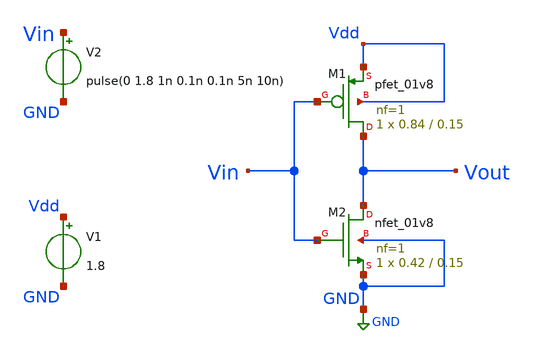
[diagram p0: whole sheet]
** sch_path: xschem_project/inverter/inverter_tb.sch
**.subckt inverter_tb
XM1 Vout Vin Vdd Vdd sky130_fd_pr__pfet_01v8 L=0.15 W=0.84 nf=1 ad='int((1 + 1)/2) * 0.84 / 1 * 0.29'
+ as='int((1 + 2)/2) * 0.84 / 1 * 0.29' pd='2*int((1 + 1)/2) * (0.84 / 1 + 0.29)' ps='2*int((1 + 2)/2) * (0.84 / 1 + 0.29)'
+ nrd='0.29 / 0.84 ' nrs='0.29 / 0.84 ' sa=0 sb=0 sd=0 mult=1 m=1
XM2 Vout Vin GND GND sky130_fd_pr__nfet_01v8 L=0.15 W=0.42 nf=1 ad='int((1 + 1)/2) * 0.42 / 1 * 0.29'
+ as='int((1 + 2)/2) * 0.42 / 1 * 0.29' pd='2*int((1 + 1)/2) * (0.42 / 1 + 0.29)' ps='2*int((1 + 2)/2) * (0.42 / 1 + 0.29)'
+ nrd='0.29 / 0.42 ' nrs='0.29 / 0.42 ' sa=0 sb=0 sd=0 mult=1 m=1
V1 Vdd GND 1.8
V2 Vin GND pulse(0 1.8 1n 0.1n 0.1n 5n 10n)
**** begin user architecture code

.lib /home/akshit/.ciel/ciel/sky130/versions/1689ac3f2dc763876eaf967227c7dfe831b031ae/sky130A/libs.tech/ngspice/sky130.lib.spice tt
.tran 0.1n 20n
.measure tran tphl TRIG v(vin) VAL=0.9 RISE=1 TARG v(vout) VAL=0.9 FALL=1
.measure tran tplh TRIG v(vin) VAL=0.9 FALL=1 TARG v(vout) VAL=0.9 RISE=1

**** end user architecture code
**.ends
.GLOBAL GND
.end
